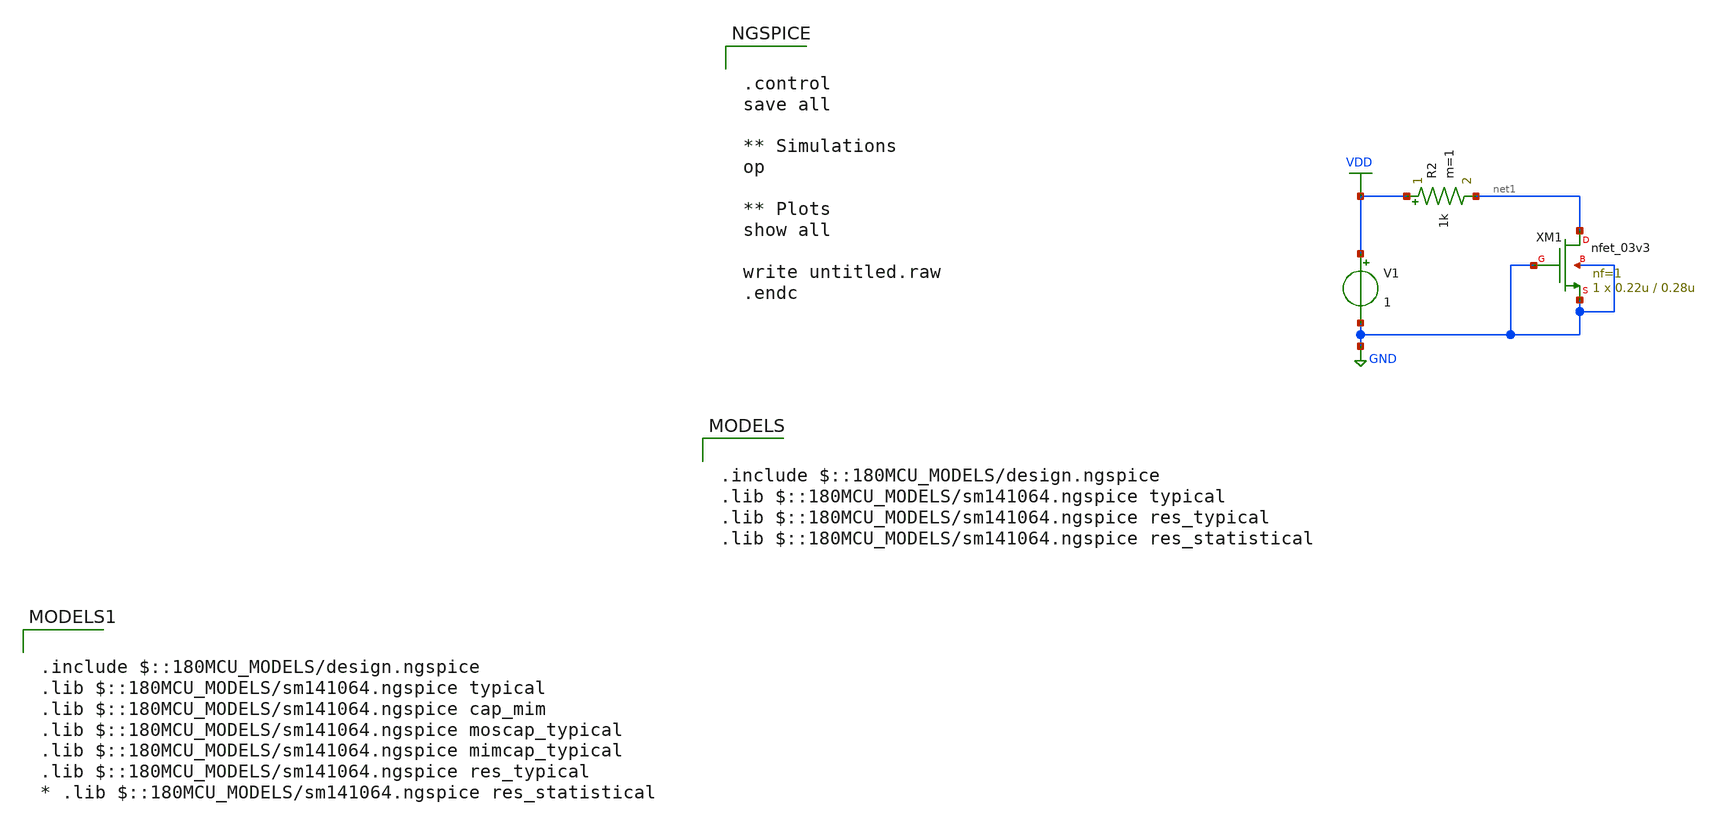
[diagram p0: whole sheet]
** sch_path: designs/untitled.sch
**.subckt untitled
V1 VDD GND 1
R2 VDD net1 1k m=1
XM1 net1 GND GND GND nfet_03v3 L=0.28u W=0.22u nf=1 ad='int((nf+1)/2) * W/nf * 0.18u' as='int((nf+2)/2) * W/nf * 0.18u'
+ pd='2*int((nf+1)/2) * (W/nf + 0.18u)' ps='2*int((nf+2)/2) * (W/nf + 0.18u)' nrd='0.18u / W' nrs='0.18u / W'
+ sa=0 sb=0 sd=0 m=1
**** begin user architecture code

.include $::180MCU_MODELS/design.ngspice
.lib $::180MCU_MODELS/sm141064.ngspice typical
.lib $::180MCU_MODELS/sm141064.ngspice res_typical
.lib $::180MCU_MODELS/sm141064.ngspice res_statistical


.include $::180MCU_MODELS/design.ngspice
.lib $::180MCU_MODELS/sm141064.ngspice typical
.lib $::180MCU_MODELS/sm141064.ngspice cap_mim
.lib $::180MCU_MODELS/sm141064.ngspice moscap_typical
.lib $::180MCU_MODELS/sm141064.ngspice mimcap_typical
.lib $::180MCU_MODELS/sm141064.ngspice res_typical
* .lib $::180MCU_MODELS/sm141064.ngspice res_statistical



.control
save all

** Simulations
op

** Plots
show all

write untitled.raw
.endc


**** end user architecture code
**.ends
.GLOBAL GND
.GLOBAL VDD
.end
